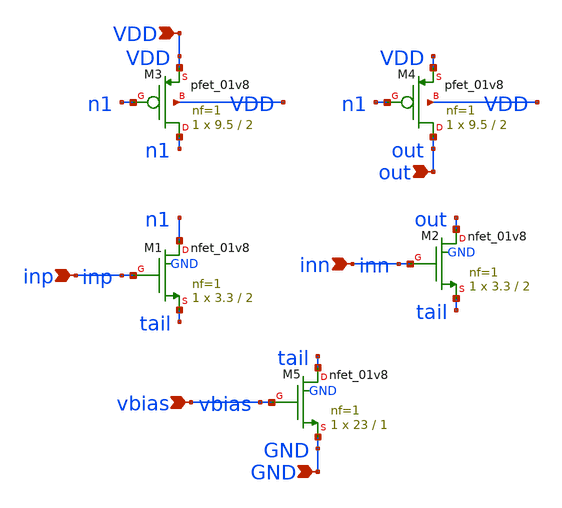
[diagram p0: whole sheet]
** sch_path: schematic/ota_5t.sch
**.subckt ota_5t inp inn vbias out VDD GND
*.ipin inp
*.ipin inn
*.ipin vbias
*.ipin out
*.ipin VDD
*.ipin GND
XM3 n1 n1 VDD VDD sky130_fd_pr__pfet_01v8 L=2 W=9.5 nf=1 ad='int((1 + 1)/2) * 9.5 / 1 * 0.29' as='int((1 + 2)/2) * 9.5 / 1 * 0.29'
+ pd='2*int((1 + 1)/2) * (9.5 / 1 + 0.29)' ps='2*int((1 + 2)/2) * (9.5 / 1 + 0.29)' nrd='0.29 / 9.5 ' nrs='0.29 / 9.5 '
+ sa=0 sb=0 sd=0 mult=1 m=1
XM4 out n1 VDD VDD sky130_fd_pr__pfet_01v8 L=2 W=9.5 nf=1 ad='int((1 + 1)/2) * 9.5 / 1 * 0.29' as='int((1 + 2)/2) * 9.5 / 1 * 0.29'
+ pd='2*int((1 + 1)/2) * (9.5 / 1 + 0.29)' ps='2*int((1 + 2)/2) * (9.5 / 1 + 0.29)' nrd='0.29 / 9.5 ' nrs='0.29 / 9.5 '
+ sa=0 sb=0 sd=0 mult=1 m=1
XM1 n1 inp tail GND sky130_fd_pr__nfet_01v8 L=2 W=3.3 nf=1 ad='int((1 + 1)/2) * 3.3 / 1 * 0.29' as='int((1 + 2)/2) * 3.3 / 1 * 0.29'
+ pd='2*int((1 + 1)/2) * (3.3 / 1 + 0.29)' ps='2*int((1 + 2)/2) * (3.3 / 1 + 0.29)' nrd='0.29 / 3.3 ' nrs='0.29 / 3.3 '
+ sa=0 sb=0 sd=0 mult=1 m=1
XM2 out inn tail GND sky130_fd_pr__nfet_01v8 L=2 W=3.3 nf=1 ad='int((1 + 1)/2) * 3.3 / 1 * 0.29' as='int((1 + 2)/2) * 3.3 / 1 * 0.29'
+ pd='2*int((1 + 1)/2) * (3.3 / 1 + 0.29)' ps='2*int((1 + 2)/2) * (3.3 / 1 + 0.29)' nrd='0.29 / 3.3 ' nrs='0.29 / 3.3 '
+ sa=0 sb=0 sd=0 mult=1 m=1
XM5 tail vbias GND GND sky130_fd_pr__nfet_01v8 L=1 W=23 nf=1 ad='int((1 + 1)/2) * 23 / 1 * 0.29' as='int((1 + 2)/2) * 23 / 1 * 0.29'
+ pd='2*int((1 + 1)/2) * (23 / 1 + 0.29)' ps='2*int((1 + 2)/2) * (23 / 1 + 0.29)' nrd='0.29 / 23 ' nrs='0.29 / 23 '
+ sa=0 sb=0 sd=0 mult=1 m=1
**.ends
.end
